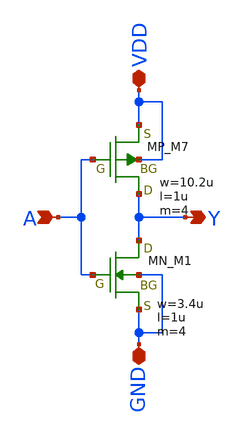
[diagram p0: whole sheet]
** sch_path: libs.tech/xschem/TR-1um_stdcell/INV_X4.sch
**.subckt INV_X4 A Y GND VDD
*.ipin A
*.opin Y
*.iopin GND
*.iopin VDD
XM7 Y A VDD VDD PMOS w=10.2u l=1u nrd=0 nrs=0 m=4
XM1 Y A GND GND NMOS w=3.4u l=1u nrd=0 nrs=0 m=4
**.ends
.end
